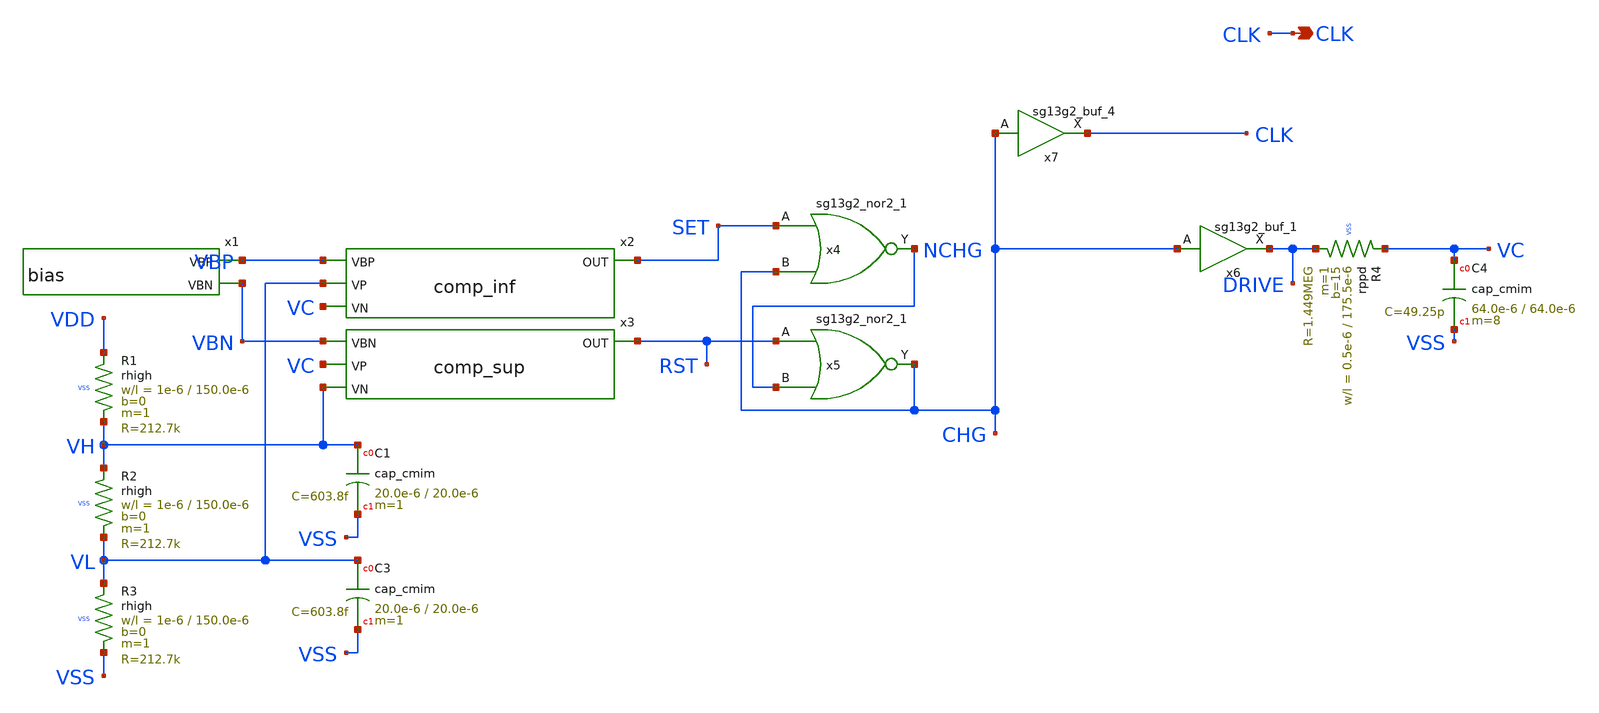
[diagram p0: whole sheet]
** sch_path: design/blocks/oscillator/schematic/wd_oscillater.sch
* IHP-GmbH/IHP-Open-PDK/ihp-sg13g2/libs.tech/xschem/sg13g2_stdcells/sg13g2_buf_1.sch:
* Copyright 2023 IHP PDK Authors
* Licensed under the Apache License, Version 2.0 (the "License");
**.subckt wd_oscillater CLK
*.opin CLK
x1 VBP VBN VDD VSS bias
x2 VBP VL VC SET VDD VSS comp_inf
x3 VBN VC VH RST VDD VSS comp_sup
XR1 VDD VH VSS rhigh w=1e-6 l=150.0e-6 m=1 b=0 mm_ok=1
XR2 VH VL VSS rhigh w=1e-6 l=150.0e-6 m=1 b=0 mm_ok=1
XR3 VL VSS VSS rhigh w=1e-6 l=150.0e-6 m=1 b=0 mm_ok=1
x4 NCHG SET CHG VDD VSS sg13g2_nor2_1
x5 CHG RST NCHG VDD VSS sg13g2_nor2_1
x6 DRIVE CHG VDD VSS sg13g2_buf_1
x7 CLK CHG VDD VSS sg13g2_buf_4
XR4 VC DRIVE VSS rppd w=0.5e-6 l=175.5e-6 m=1 b=15 mm_ok=1
XC1 VH VSS cap_cmim w=20.0e-6 l=20.0e-6 m=1 mm_ok=1
XC3 VL VSS cap_cmim w=20.0e-6 l=20.0e-6 m=1 mm_ok=1
XC4 VC VSS cap_cmim w=64.0e-6 l=64.0e-6 m=8 mm_ok=1
**.ends

* expanding   symbol:  bias.sym # of pins=2
** sym_path: design/blocks/bias/schematic/bias.sym
** sch_path: design/blocks/bias/schematic/bias.sch
.subckt bias VBP VBN VDD VSS
*.opin VBP
*.opin VBN
XM1 VBN VBN VSS VSS sg13_lv_nmos w=2u l=1u ng=1 m=1 mm_ok=1
XM2 VBP VBP VDD VDD sg13_lv_pmos w=2u l=1u ng=1 m=1 mm_ok=1
XR2 VBP VSS VSS rhigh w=0.5e-6 l=10.0e-6 m=1 b=0 mm_ok=1
XR1 VDD VBN VSS rhigh w=0.5e-6 l=10.0e-6 m=1 b=0 mm_ok=1
XC1 VBN VSS cap_cmim w=26.0e-6 l=26.0e-6 m=1 mm_ok=1
XC2 VDD VBP cap_cmim w=26.0e-6 l=26.0e-6 m=1 mm_ok=1
.ends


* expanding   symbol:  comp_inf.sym # of pins=4
** sym_path: design/blocks/comparator/schematic/comp_inf.sym
** sch_path: design/blocks/comparator/schematic/comp_inf.sch
.subckt comp_inf VBP VP VN OUT VDD VSS
*.opin OUT
*.ipin VN
*.ipin VP
*.ipin VBP
XM1 TAIL VBP VDD VDD sg13_lv_pmos w=4u l=4u ng=1 m=1 mm_ok=1
XM7 DIO VP TAIL VDD sg13_lv_pmos w=20u l=1u ng=4 m=1 mm_ok=1
XM8 OUT1 VN TAIL VDD sg13_lv_pmos w=20u l=1u ng=4 m=1 mm_ok=1
XM9 DIO DIO VSS VSS sg13_lv_nmos w=1u l=8u ng=1 m=1 mm_ok=1
XM10 OUT1 DIO VSS VSS sg13_lv_nmos w=1u l=8u ng=1 m=1 mm_ok=1
XM2 OUT2 VBP VDD VDD sg13_lv_pmos w=4u l=4u ng=1 m=1 mm_ok=1
XM3 OUT2 OUT1 VSS VSS sg13_lv_nmos w=2u l=8u ng=1 m=1 mm_ok=1
x1 OUT2 OUT VDD VSS schmitt
.ends


* expanding   symbol:  comp_sup.sym # of pins=4
** sym_path: design/blocks/comparator/schematic/comp_sup.sym
** sch_path: design/blocks/comparator/schematic/comp_sup.sch
.subckt comp_sup VBN VP VN OUT VDD VSS
*.opin OUT
*.ipin VN
*.ipin VP
*.ipin VBN
XM2 DIO DIO VDD VDD sg13_lv_pmos w=2u l=4u ng=1 m=1 mm_ok=1
XM3 OUT1 DIO VDD VDD sg13_lv_pmos w=2u l=4u ng=1 m=1 mm_ok=1
XM4 DIO VP TAIL VSS sg13_lv_nmos w=20u l=2u ng=4 m=1 mm_ok=1
XM5 OUT1 VN TAIL VSS sg13_lv_nmos w=20u l=2u ng=4 m=1 mm_ok=1
XM6 TAIL VBN VSS VSS sg13_lv_nmos w=2u l=4u ng=1 m=1 mm_ok=1
XM1 OUT2 OUT1 VDD VDD sg13_lv_pmos w=4u l=4u ng=1 m=1 mm_ok=1
XM7 OUT2 VBN VSS VSS sg13_lv_nmos w=2u l=4u ng=1 m=1 mm_ok=1
x1 OUT2 OUT VDD VSS schmitt
.ends


* expanding   symbol:  sg13g2_nor2_1.sym # of pins=3
** sym_path: sg13g2_nor2_1.sym
** sch_path: sg13g2_nor2_1.sch
.subckt sg13g2_nor2_1 Y A B VDD VSS
*.opin Y
*.ipin B
*.ipin A
*.iopin VDD
*.iopin VSS
XM1 Y A VSS VSS sg13_lv_nmos w=740.00n l=130.00n ng=1 m=1 mm_ok=1
XM2 Y B VSS VSS sg13_lv_nmos w=740.00n l=130.00n ng=1 m=1 mm_ok=1
XM3 net1 A VDD VDD sg13_lv_pmos w=1.12u l=130.00n ng=1 m=1 mm_ok=1
XM4 Y B net1 VDD sg13_lv_pmos w=1.12u l=130.00n ng=1 m=1 mm_ok=1
.ends


* expanding   symbol:  sg13g2_buf_1.sym # of pins=2
** sym_path: sg13g2_buf_1.sym
** sch_path: sg13g2_buf_1.sch
.subckt sg13g2_buf_1 X A VDD VSS
*.ipin A
*.opin X
*.iopin VDD
*.iopin VSS
XM1 net1 A VSS VSS sg13_lv_nmos w=550.00n l=130.00n ng=1 m=1 mm_ok=1
XM2 X net1 VSS VSS sg13_lv_nmos w=740.00n l=130.00n ng=1 m=1 mm_ok=1
XM3 net1 A VDD VDD sg13_lv_pmos w=840.00n l=130.00n ng=1 m=1 mm_ok=1
XM4 X net1 VDD VDD sg13_lv_pmos w=1.12u l=130.00n ng=1 m=1 mm_ok=1
.ends


* expanding   symbol:  sg13g2_buf_4.sym # of pins=2
** sym_path: sg13g2_buf_4.sym
** sch_path: sg13g2_buf_4.sch
.subckt sg13g2_buf_4 X A VDD VSS
*.ipin A
*.opin X
*.iopin VDD
*.iopin VSS
XM1 net1 A VSS VSS sg13_lv_nmos w=740.00n l=130.00n ng=1 m=1 mm_ok=1
XM2 X net1 VSS VSS sg13_lv_nmos w=2.96u l=130.00n ng=4 m=1 mm_ok=1
XM3 net1 A VDD VDD sg13_lv_pmos w=1.68u l=130.00n ng=2 m=1 mm_ok=1
XM4 X net1 VDD VDD sg13_lv_pmos w=4.48u l=130.00n ng=4 m=1 mm_ok=1
.ends


* expanding   symbol:  schmitt.sym # of pins=2
** sym_path: design/blocks/schmitt/schematic/schmitt.sym
** sch_path: design/blocks/schmitt/schematic/schmitt.sch
.subckt schmitt IN OUT VDD VSS
*.opin OUT
*.ipin IN
XM4 P_MID IN VDD VDD sg13_lv_pmos w=1.04u l=0.13u ng=1 m=1 mm_ok=1
XM6 OUT IN N_MID VSS sg13_lv_nmos w=0.76u l=0.13u ng=1 m=1 mm_ok=1
XM5 OUT IN P_MID VDD sg13_lv_pmos w=1.04u l=0.13u ng=1 m=1 mm_ok=1
XM7 N_MID IN VSS VSS sg13_lv_nmos w=0.76u l=0.13u ng=1 m=1 mm_ok=1
XM8 VSS OUT P_MID VDD sg13_lv_pmos w=0.42u l=0.13u ng=1 m=1 mm_ok=1
XM9 VDD OUT N_MID VSS sg13_lv_nmos w=0.42u l=0.13u ng=1 m=1 mm_ok=1
.ends

.end
